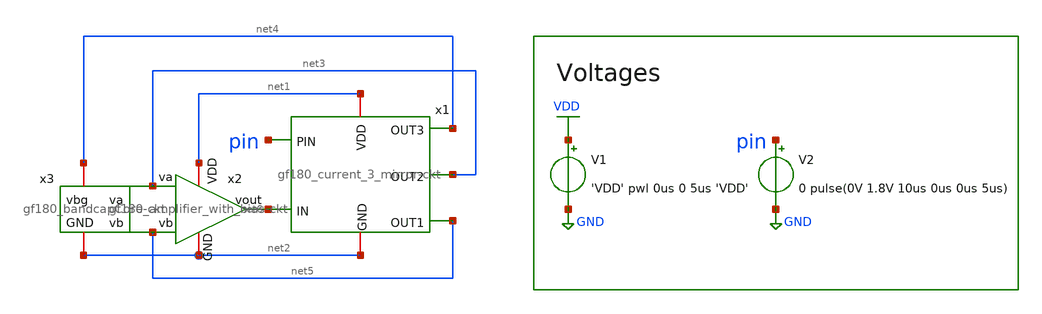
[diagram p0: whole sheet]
** sch_path: gf180_bandgap_real_op.sch
**.subckt gf180_bandgap_real_op
x1 net6 pin net5 net3 net4 net1 net2 gf180_current_3_mirror-ckt
x2 net3 net5 net6 net1 net2 gf180_amplifier_with_bias-ckt
x3 net3 net5 net4 net2 gf180_bandcapCore-ckt
V1 VDD GND 'VDD' pwl 0us 0 5us 'VDD'
V2 pin GND 0 pulse(0V 1.8V 10us 0us 0us 5us)
**** begin user architecture code

** opencircuitdesign pdks install
.lib $::SKYWATER_MODELS/sky130.lib.spice tt


**** end user architecture code
**.ends

* expanding   symbol:
*+  /home/thomas/Projects/HW-Design/ieee_comps/bandgap_01_gf180mcu/gf180_current_3_mirror-ckt.sym # of pins=7
** sym_path: gf180_current_3_mirror-ckt.sym
** sch_path: gf180_current_3_mirror-ckt.sch
.subckt gf180_current_3_mirror-ckt IN PIN OUT1 OUT2 OUT3 VDD GND
*.ipin IN
*.opin OUT2
*.iopin VDD
*.iopin GND
*.opin OUT3
*.opin OUT1
*.ipin PIN
XM1 OUT1 IN VDD VDD pfet_03v3 L=0.28u W=0.22u nf=1 ad='int((nf+1)/2) * W/nf * 0.18u' as='int((nf+2)/2) * W/nf * 0.18u'
+ pd='2*int((nf+1)/2) * (W/nf + 0.18u)' ps='2*int((nf+2)/2) * (W/nf + 0.18u)' nrd='0.18u / W' nrs='0.18u / W'
+ sa=0 sb=0 sd=0 m=1
XM2 OUT2 IN VDD VDD pfet_03v3 L=0.28u W=0.22u nf=1 ad='int((nf+1)/2) * W/nf * 0.18u' as='int((nf+2)/2) * W/nf * 0.18u'
+ pd='2*int((nf+1)/2) * (W/nf + 0.18u)' ps='2*int((nf+2)/2) * (W/nf + 0.18u)' nrd='0.18u / W' nrs='0.18u / W'
+ sa=0 sb=0 sd=0 m=1
XM3 IN PIN GND GND nfet_03v3 L=0.28u W=0.22u nf=1 ad='int((nf+1)/2) * W/nf * 0.18u' as='int((nf+2)/2) * W/nf * 0.18u'
+ pd='2*int((nf+1)/2) * (W/nf + 0.18u)' ps='2*int((nf+2)/2) * (W/nf + 0.18u)' nrd='0.18u / W' nrs='0.18u / W'
+ sa=0 sb=0 sd=0 m=1
XM4 OUT3 IN VDD VDD nfet_03v3 L=0.28u W=0.22u nf=1 ad='int((nf+1)/2) * W/nf * 0.18u' as='int((nf+2)/2) * W/nf * 0.18u'
+ pd='2*int((nf+1)/2) * (W/nf + 0.18u)' ps='2*int((nf+2)/2) * (W/nf + 0.18u)' nrd='0.18u / W' nrs='0.18u / W'
+ sa=0 sb=0 sd=0 m=1
XC1 VDD IN cap_mim_2p0fF c_width=1e-6 c_length=1e-6 m=1
.ends


* expanding   symbol:
*+  /home/thomas/Projects/HW-Design/ieee_comps/bandgap_01_gf180mcu/gf180_amplifier_with_bias-ckt.sym # of pins=5
** sym_path: gf180_amplifier_with_bias-ckt.sym
** sch_path: gf180_amplifier_with_bias-ckt.sch
.subckt gf180_amplifier_with_bias-ckt va vb vout VDD GND
*.ipin va
*.iopin VDD
*.ipin vb
*.opin vout
*.iopin GND
XM1 VDD vg vg VDD pfet_03v3 L=0.28u W=0.22u nf=1 ad='int((nf+1)/2) * W/nf * 0.18u' as='int((nf+2)/2) * W/nf * 0.18u'
+ pd='2*int((nf+1)/2) * (W/nf + 0.18u)' ps='2*int((nf+2)/2) * (W/nf + 0.18u)' nrd='0.18u / W' nrs='0.18u / W'
+ sa=0 sb=0 sd=0 m=1
XM2 vout vg VDD VDD pfet_03v3 L=0.28u W=0.22u nf=1 ad='int((nf+1)/2) * W/nf * 0.18u' as='int((nf+2)/2) * W/nf * 0.18u'
+ pd='2*int((nf+1)/2) * (W/nf + 0.18u)' ps='2*int((nf+2)/2) * (W/nf + 0.18u)' nrd='0.18u / W' nrs='0.18u / W'
+ sa=0 sb=0 sd=0 m=1
XM3 vg va vq GND nfet_03v3 L=0.28u W=0.22u nf=1 ad='int((nf+1)/2) * W/nf * 0.18u' as='int((nf+2)/2) * W/nf * 0.18u'
+ pd='2*int((nf+1)/2) * (W/nf + 0.18u)' ps='2*int((nf+2)/2) * (W/nf + 0.18u)' nrd='0.18u / W' nrs='0.18u / W'
+ sa=0 sb=0 sd=0 m=1
XM4 vq vb vout GND nfet_03v3 L=0.28u W=0.22u nf=1 ad='int((nf+1)/2) * W/nf * 0.18u' as='int((nf+2)/2) * W/nf * 0.18u'
+ pd='2*int((nf+1)/2) * (W/nf + 0.18u)' ps='2*int((nf+2)/2) * (W/nf + 0.18u)' nrd='0.18u / W' nrs='0.18u / W'
+ sa=0 sb=0 sd=0 m=1
XM5 vq net1 GND GND nfet_03v3 L=0.28u W=0.22u nf=1 ad='int((nf+1)/2) * W/nf * 0.18u' as='int((nf+2)/2) * W/nf * 0.18u'
+ pd='2*int((nf+1)/2) * (W/nf + 0.18u)' ps='2*int((nf+2)/2) * (W/nf + 0.18u)' nrd='0.18u / W' nrs='0.18u / W'
+ sa=0 sb=0 sd=0 m=1
XM6 net1 net1 GND GND nfet_03v3 L=0.28u W=0.22u nf=1 ad='int((nf+1)/2) * W/nf * 0.18u' as='int((nf+2)/2) * W/nf * 0.18u'
+ pd='2*int((nf+1)/2) * (W/nf + 0.18u)' ps='2*int((nf+2)/2) * (W/nf + 0.18u)' nrd='0.18u / W' nrs='0.18u / W'
+ sa=0 sb=0 sd=0 m=1
XM8 net1 vout VDD VDD pfet_03v3 L=0.28u W=0.22u nf=1 ad='int((nf+1)/2) * W/nf * 0.18u' as='int((nf+2)/2) * W/nf * 0.18u'
+ pd='2*int((nf+1)/2) * (W/nf + 0.18u)' ps='2*int((nf+2)/2) * (W/nf + 0.18u)' nrd='0.18u / W' nrs='0.18u / W'
+ sa=0 sb=0 sd=0 m=1
.ends


* expanding   symbol:
*+  /home/thomas/Projects/HW-Design/ieee_comps/bandgap_01_gf180mcu/gf180_bandcapCore-ckt.sym # of pins=4
** sym_path: gf180_bandcapCore-ckt.sym
** sch_path: gf180_bandcapCore-ckt.sch
.subckt gf180_bandcapCore-ckt va vb vbg GND
*.ipin va
*.ipin vb
*.iopin vbg
*.iopin GND
XQ1 GND GND veb vpbp_10x10 m=1
XQ2 GND GND vbneg vpbp_10x10 m=1
XR1 vbneg net2 GND nplus_u r_width=1e-6 r_length=1e-6 m=1
XR2 GND net3 GND nplus_u r_width=1e-6 r_length=1e-6 m=1
XR3 GND vbg GND nplus_u r_width=1e-6 r_length=1e-6 m=1
XR4 GND net1 GND nplus_u r_width=1e-6 r_length=1e-6 m=1
Vr4 vb net2 0
.save i(vr4)
Vr1 vb net3 0
.save i(vr1)
Vr2 va net1 0
.save i(vr2)
Vr3 va veb 0
.save i(vr3)
.ends

.GLOBAL VDD
.GLOBAL GND
.end
